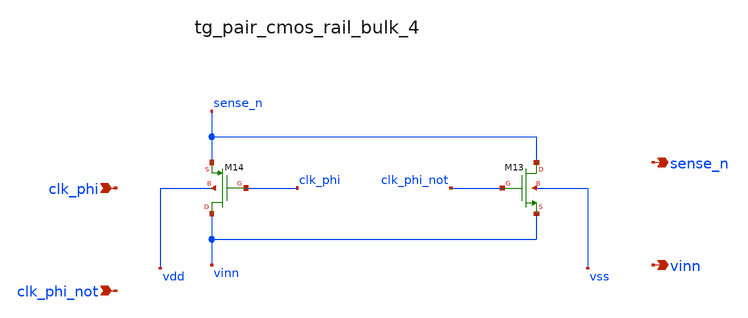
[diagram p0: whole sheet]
** sch_path: analog-db/raw/cmfb_004_output_switched_cap/hier/blocks/tg_pair_cmos_rail_bulk_4.sch
**.subckt tg_pair_cmos_rail_bulk_4 clk_phi clk_phi_not sense_n vinn
*.ipin clk_phi
*.ipin clk_phi_not
*.opin sense_n
*.opin vinn
XM13 sense_n clk_phi_not vinn vss sg13_lv_nmos w=x_dut_xm13_w l=x_dut_xm13_l ng=1 m=x_dut_xm13_m
XM14 vinn clk_phi sense_n vdd sg13_lv_pmos w=x_dut_xm14_w l=x_dut_xm14_l ng=1 m=x_dut_xm14_m
**.ends
.end
